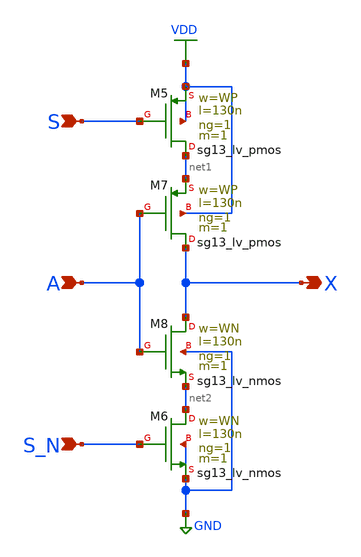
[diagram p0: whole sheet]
** sch_path: Tile/include/cmos5l/konrads_cells/sch/tri_buff.sch
**.subckt tri_buff A S S_N X
*.ipin A
*.ipin S
*.ipin S_N
*.opin X
XM5 net1 S VDD VDD sg13_lv_pmos w=WP l=130n ng=1 m=1 mm_ok=1
XM6 net2 S_N GND GND sg13_lv_nmos w=WN l=130n ng=1 m=1 mm_ok=1
XM7 X A net1 VDD sg13_lv_pmos w=WP l=130n ng=1 m=1 mm_ok=1
XM8 X A net2 GND sg13_lv_nmos w=WN l=130n ng=1 m=1 mm_ok=1
**.ends
.GLOBAL VDD
.GLOBAL GND
.end
